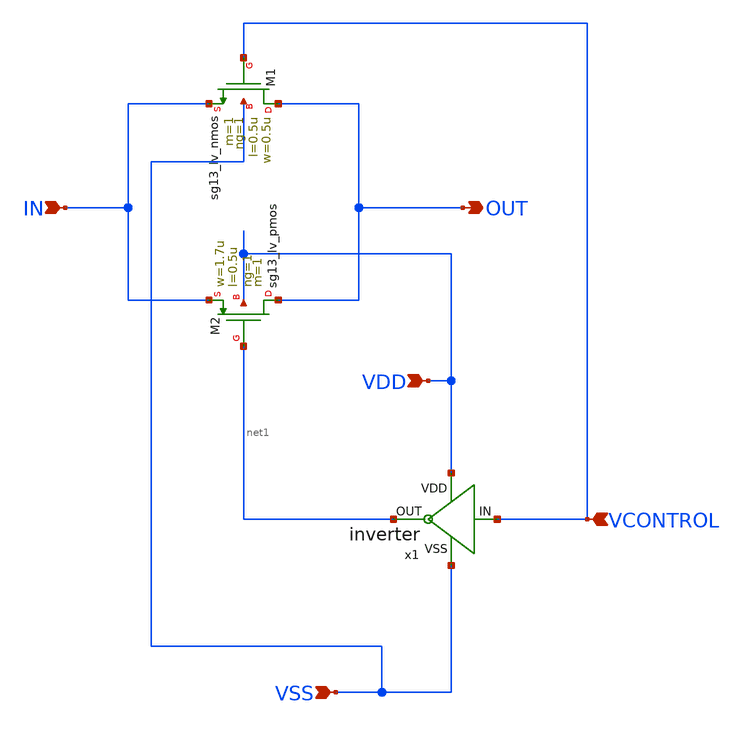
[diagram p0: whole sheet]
** sch_path: transmission-gate/switch.sch
**.subckt switch IN VDD VSS VCONTROL OUT
*.ipin IN
*.ipin VDD
*.ipin VSS
*.ipin VCONTROL
*.opin OUT
XM1 OUT VCONTROL IN VSS sg13_lv_nmos w=0.5u l=0.5u ng=1 m=1 mm_ok=1
XM2 OUT net1 IN VDD sg13_lv_pmos w=1.7u l=0.5u ng=1 m=1 mm_ok=1
x1 VDD VCONTROL net1 VSS inverter
**.ends
.end
